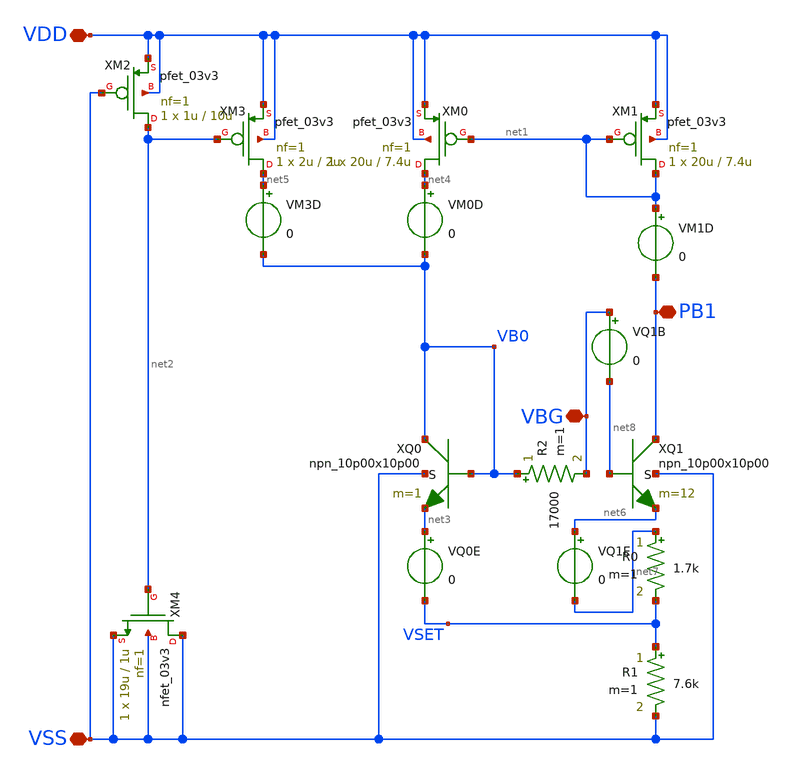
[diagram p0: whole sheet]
** sch_path: bandgap/cace/testbenches/bandgap.sch
**.subckt bandgap VSS VDD PB1 VBG
*.iopin VSS
*.iopin VDD
*.iopin PB1
*.iopin VBG
R0 net7 VSET 1.7k m=1
R1 VSET VSS 7.6k m=1
R2 VB0 VBG 17000 m=1
XQ1 PB1 net8 net6 VSS npn_10p00x10p00 m=12
XQ0 VB0 VB0 net3 VSS npn_10p00x10p00 m=1
XM4 VSS net2 VSS VSS nfet_03v3 L=1u W=19u nf=1 ad='int((nf+1)/2) * W/nf * 0.18u' as='int((nf+2)/2) * W/nf * 0.18u'
+ pd='2*int((nf+1)/2) * (W/nf + 0.18u)' ps='2*int((nf+2)/2) * (W/nf + 0.18u)' nrd='0.18u / W' nrs='0.18u / W'
+ sa=0 sb=0 sd=0 m=1
XM2 net2 VSS VDD VDD pfet_03v3 L=10u W=1u nf=1 ad='int((nf+1)/2) * W/nf * 0.18u' as='int((nf+2)/2) * W/nf * 0.18u'
+ pd='2*int((nf+1)/2) * (W/nf + 0.18u)' ps='2*int((nf+2)/2) * (W/nf + 0.18u)' nrd='0.18u / W' nrs='0.18u / W'
+ sa=0 sb=0 sd=0 m=1
XM3 net5 net2 VDD VDD pfet_03v3 L=2u W=2u nf=1 ad='int((nf+1)/2) * W/nf * 0.18u' as='int((nf+2)/2) * W/nf * 0.18u'
+ pd='2*int((nf+1)/2) * (W/nf + 0.18u)' ps='2*int((nf+2)/2) * (W/nf + 0.18u)' nrd='0.18u / W' nrs='0.18u / W'
+ sa=0 sb=0 sd=0 m=1
XM1 net1 net1 VDD VDD pfet_03v3 L=7.4u W=20u nf=1 ad='int((nf+1)/2) * W/nf * 0.18u' as='int((nf+2)/2) * W/nf * 0.18u'
+ pd='2*int((nf+1)/2) * (W/nf + 0.18u)' ps='2*int((nf+2)/2) * (W/nf + 0.18u)' nrd='0.18u / W' nrs='0.18u / W'
+ sa=0 sb=0 sd=0 m=1
XM0 net4 net1 VDD VDD pfet_03v3 L=7.4u W=20u nf=1 ad='int((nf+1)/2) * W/nf * 0.18u' as='int((nf+2)/2) * W/nf * 0.18u'
+ pd='2*int((nf+1)/2) * (W/nf + 0.18u)' ps='2*int((nf+2)/2) * (W/nf + 0.18u)' nrd='0.18u / W' nrs='0.18u / W'
+ sa=0 sb=0 sd=0 m=1
VQ0E net3 VSET 0
VM0D net4 VB0 0
VM3D net5 VB0 0
VQ1E net6 net7 0
VM1D net1 PB1 0
VQ1B VBG net8 0
**.ends
.end
